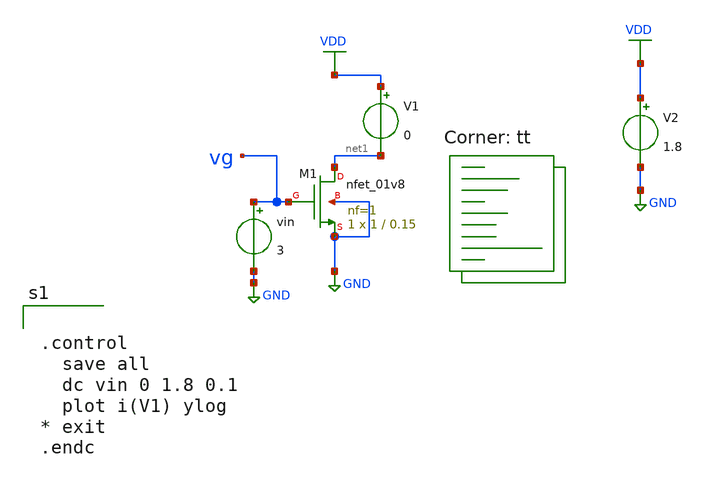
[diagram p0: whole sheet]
** sch_path: project2/test_schem.sch
**.subckt test_schem
XM1 net1 vg GND GND sky130_fd_pr__nfet_01v8 L=0.15 W=1 nf=1 ad='int((nf+1)/2) * W/nf * 0.29' as='int((nf+2)/2) * W/nf * 0.29'
+ pd='2*int((nf+1)/2) * (W/nf + 0.29)' ps='2*int((nf+2)/2) * (W/nf + 0.29)' nrd='0.29 / W' nrs='0.29 / W'
+ sa=0 sb=0 sd=0 mult=1 m=1
vin vg GND 3
V1 VDD net1 0
V2 VDD GND 1.8
**** begin user architecture code
.lib $::SKYWATER_MODELS/sky130.lib.spice tt


.control
  save all
  dc vin 0 1.8 0.1
  plot i(V1) ylog
* exit
.endc


**** end user architecture code
**.ends
.GLOBAL GND
.GLOBAL VDD
.end
